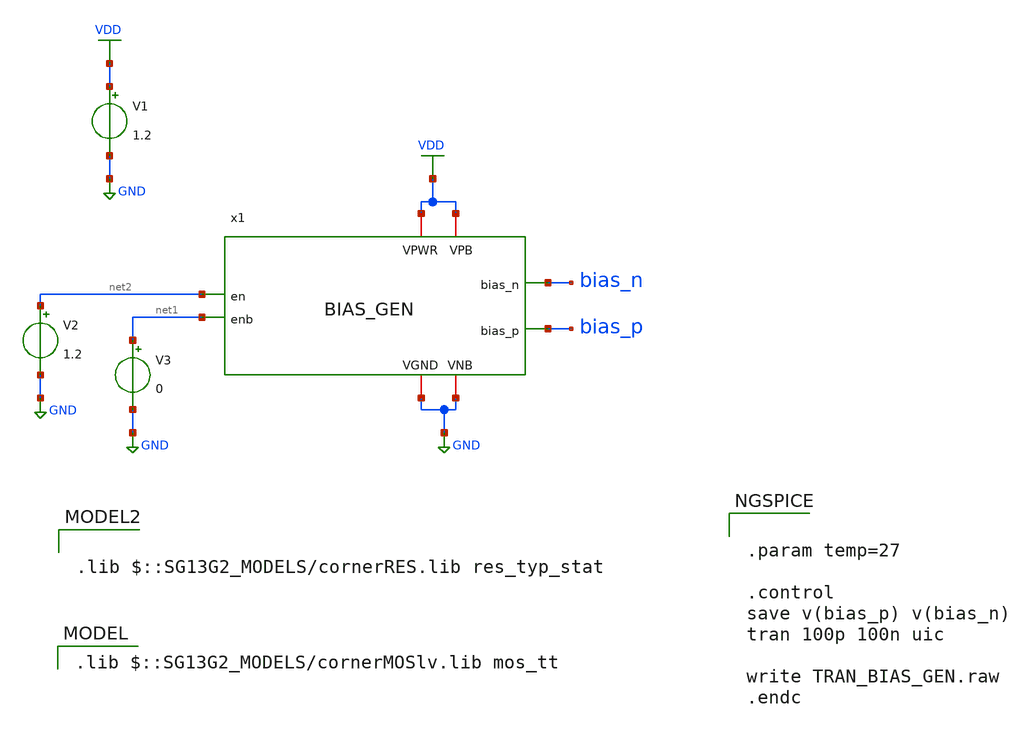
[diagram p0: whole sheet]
** sch_path: 30_MHz_Fractional_N_PLL/design_data/xschem/BIAS_GEN_TB.sch
**.subckt BIAS_GEN_TB
x1 VDD VDD GND GND net2 bias_n bias_p net1 BIAS_GEN
V1 VDD GND 1.2
V2 net2 GND 1.2
V3 net1 GND 0
**** begin user architecture code


.param temp=27

.control
save v(bias_p) v(bias_n)
tran 100p 100n uic

write TRAN_BIAS_GEN.raw
.endc


 .lib $::SG13G2_MODELS/cornerMOSlv.lib mos_tt


.lib $::SG13G2_MODELS/cornerRES.lib res_typ_stat

**** end user architecture code
**.ends

* expanding   symbol:  BIAS_GEN.sym # of pins=8
** sym_path: 30_MHz_Fractional_N_PLL/design_data/xschem/BIAS_GEN.sym
** sch_path: 30_MHz_Fractional_N_PLL/design_data/xschem/BIAS_GEN.sch
.subckt BIAS_GEN VPWR VPB VGND VNB en bias_n bias_p enb
*.ipin en
*.opin bias_n
*.iopin VNB
*.iopin VGND
*.iopin VPB
*.iopin VPWR
*.ipin enb
*.opin bias_p
XM1 bias_p kick kick_sw VNB sg13_lv_nmos w=0.5u l=0.15u ng=1 m=1 mm_ok=1
XM2 kick_sw en VGND VNB sg13_lv_nmos w=0.5u l=0.15u ng=1 m=1 mm_ok=1
XM3 kick bias_n VGND VNB sg13_lv_nmos w=1.0u l=1.0u ng=1 m=1 mm_ok=1
XM4 bias_p bias_n net1 VNB sg13_lv_nmos w=1.0u l=1.0u ng=1 m=1 mm_ok=1
XM5 bias_n enb VGND VNB sg13_lv_nmos w=0.5u l=0.15u ng=1 m=1 mm_ok=1
XM6 bias_n bias_n VGND VNB sg13_lv_nmos w=1.0u l=1.0u ng=1 m=1 mm_ok=1
XM7 kick kick dio_mid VPB sg13_lv_pmos w=0.5u l=0.15u ng=1 m=1 mm_ok=1
XM8 bias_p bias_p VPWR VPB sg13_lv_pmos w=2.0u l=1.0u ng=1 m=1 mm_ok=1
XM9 bias_p en VPWR VPB sg13_lv_pmos w=0.5u l=0.15u ng=1 m=1 mm_ok=1
XM10 bias_n bias_p res_bot VPB sg13_lv_pmos w=4.0u l=1.0u ng=1 m=1 mm_ok=1
XM11 kick en VPWR VPB sg13_lv_pmos w=0.5u l=0.15u ng=1 m=1 mm_ok=1
XM12 dio_mid dio_mid VPWR VPB sg13_lv_pmos w=0.5u l=0.15u ng=1 m=1 mm_ok=1
XR1 VPWR res_bot sub! rhigh w=1.0e-6 l=12.0e-6 m=1 b=0 mm_ok=1
XR2 net1 VGND sub! rhigh w=1.0e-6 l=12.0e-6 m=1 b=0 mm_ok=1
.ends

.GLOBAL GND
.GLOBAL VDD
.end
